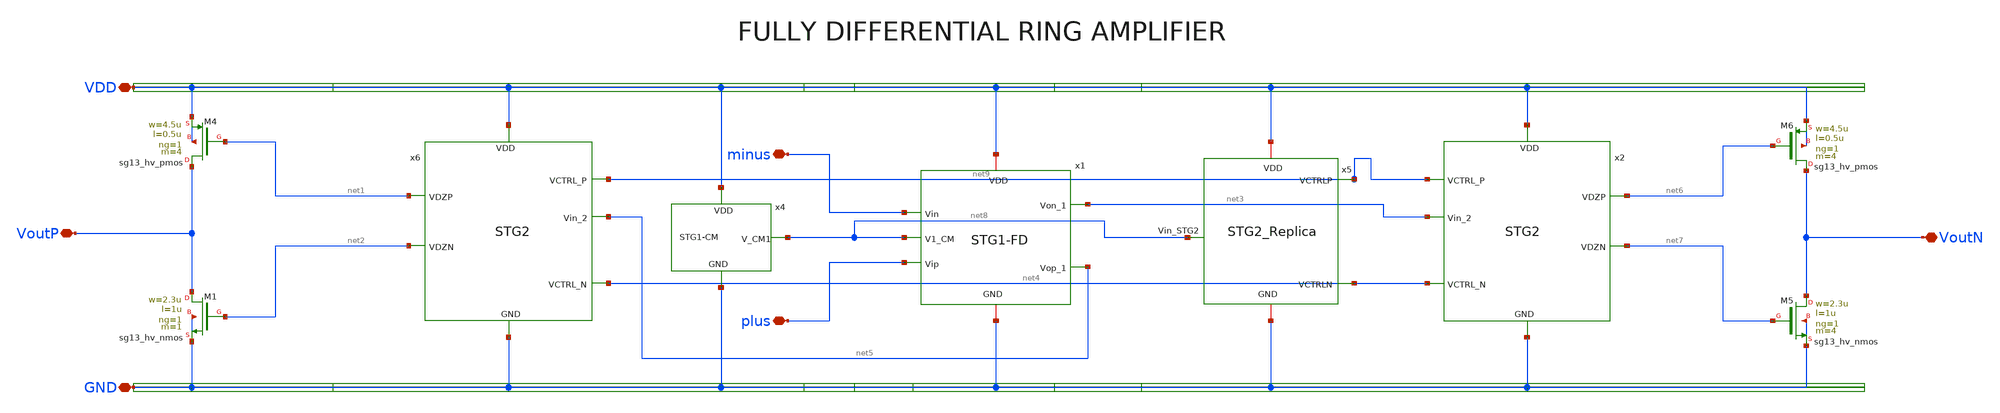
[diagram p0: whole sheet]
** sch_path: Design Files/RAMP/Fully-Diff-RAMP/RAMP-FD.sch
**.subckt RAMP-FD GND VDD plus minus VoutP VoutN
*.iopin GND
*.iopin VDD
*.iopin plus
*.iopin minus
*.iopin VoutP
*.iopin VoutN
x2 VDD net9 net6 net3 net7 net4 GND STG2
XM1 VoutP net2 GND GND sg13_hv_nmos w=2.3u l=1u ng=1 m=1 mm_ok=1
XM4 VoutP net1 VDD VDD sg13_hv_pmos w=4.5u l=0.5u ng=1 m=4 mm_ok=1
x1 VDD net3 net5 net8 minus plus GND STG1-FD
x4 VDD net8 GND STG1-CM
x5 VDD net9 net8 net4 GND STG2_Replica
x6 VDD net9 net1 net5 net2 net4 GND STG2
XM5 VoutN net7 GND GND sg13_hv_nmos w=2.3u l=1u ng=1 m=4 mm_ok=1
XM6 VoutN net6 VDD VDD sg13_hv_pmos w=4.5u l=0.5u ng=1 m=4 mm_ok=1
**.ends

* expanding   symbol:  /foss/designs/RAMP/Fully-Diff-RAMP/STG2.sym # of pins=7
** sym_path: Design Files/RAMP/Fully-Diff-RAMP/STG2.sym
** sch_path: Design Files/RAMP/Fully-Diff-RAMP/STG2.sch
.subckt STG2 VDD VCTRL_P VDZP Vin_2 VDZN VCTRL_N GND
*.ipin Vin_2
*.ipin VDD
*.ipin GND
*.ipin VCTRL_P
*.ipin VCTRL_N
*.opin VDZN
*.opin VDZP
XMN_STG2_3N1 VDZN Vin_2 GND GND sg13_lv_nmos w=0.15u l=0.13u ng=1 m=1 mm_ok=1
XMN_STG2_3P1 VDZN Vin_2 net1 VDD sg13_lv_pmos w=0.15u l=0.13u ng=1 m=3 mm_ok=1
XMP_DZ_STG2_3N net1 VCTRL_P VDD VDD sg13_lv_pmos w=0.15u l=0.13u ng=1 m=5 mm_ok=1
XMP_STG2_3P2 VDZP Vin_2 net2 net2 sg13_lv_nmos w=0.15u l=0.13u ng=1 m=1 mm_ok=1
XMP_STG2_3P1 VDZP Vin_2 VDD VDD sg13_lv_pmos w=0.15u l=0.13u ng=1 m=1 mm_ok=1
XMN_DZ_STG2_3P net2 VCTRL_N GND GND sg13_lv_nmos w=0.15u l=0.13u ng=1 m=1 mm_ok=1
.ends


* expanding   symbol:  /foss/designs/RAMP/Fully-Diff-RAMP/STG1-FD.sym # of pins=7
** sym_path: Design Files/RAMP/Fully-Diff-RAMP/STG1-FD.sym
** sch_path: Design Files/RAMP/Fully-Diff-RAMP/STG1-FD.sch
.subckt STG1-FD VDD Von_1 Vop_1 V1_CM Vin Vip GND
*.opin Von_1
*.iopin VDD
*.iopin GND
*.opin Vop_1
*.ipin Vip
*.ipin Vin
*.ipin V1_CM
R1 net2 Von_1 100k m=1
R3 net2 Vop_1 100k m=1
XMN_STG1_IP_N1 Von_1 Vip net3 GND sg13_lv_nmos w=1.563u l=0.5u ng=1 m=2 mm_ok=1
XMN_STG1_IP_N2 Vop_1 Vin net3 GND sg13_lv_nmos w=1.563u l=0.5u ng=1 m=2 mm_ok=1
I0 net3 GND 10u
XMP_STG1_CL_P1 Von_1 net1 VDD VDD sg13_hv_pmos w=0.5u l=1u ng=1 m=1 mm_ok=1
XMP_STG1_CL_P2 Vop_1 net1 VDD VDD sg13_hv_pmos w=0.5u l=1u ng=1 m=1 mm_ok=1
E1 net1 GND net2 V1_CM 10k
.ends


* expanding   symbol:  /foss/designs/RAMP/Fully-Diff-RAMP/STG1-CM.sym # of pins=3
** sym_path: Design Files/RAMP/Fully-Diff-RAMP/STG1-CM.sym
** sch_path: Design Files/RAMP/Fully-Diff-RAMP/STG1-CM.sch
.subckt STG1-CM VDD V_CM1 GND
*.ipin VDD
*.ipin GND
*.opin V_CM1
XM9 V_CM1 V_CM1 GND GND sg13_lv_nmos w=0.15u l=0.13u ng=1 m=1 mm_ok=1
XM10 V_CM1 V_CM1 net1 VDD sg13_lv_pmos w=0.15u l=0.13u ng=1 m=3 mm_ok=1
XM11 net1 GND VDD VDD sg13_lv_pmos w=0.15u l=0.13u ng=1 m=5 mm_ok=1
XM12 V_CM1 V_CM1 net2 net2 sg13_lv_nmos w=0.15u l=0.13u ng=1 m=1 mm_ok=1
XM13 V_CM1 V_CM1 VDD VDD sg13_lv_pmos w=0.15u l=0.13u ng=1 m=1 mm_ok=1
XM14 net2 VDD GND GND sg13_lv_nmos w=0.15u l=0.13u ng=1 m=1 mm_ok=1
.ends


* expanding   symbol:  /foss/designs/RAMP/Fully-Diff-RAMP/STG2_Replica.sym # of pins=5
** sym_path: Design Files/RAMP/Fully-Diff-RAMP/STG2_Replica.sym
** sch_path: Design Files/RAMP/Fully-Diff-RAMP/STG2_Replica.sch
.subckt STG2_Replica VDD VCTRLP Vin_STG2 VCTRLN GND
*.ipin Vin_STG2
*.iopin VDD
*.iopin GND
*.opin VCTRLP
*.opin VCTRLN
XMN_STG2_3N1 net1 Vin_STG2 GND GND sg13_lv_nmos w=0.15u l=0.13u ng=1 m=1 mm_ok=1
XMN_STG2_3P1 net1 Vin_STG2 net2 VDD sg13_lv_pmos w=0.15u l=0.13u ng=1 m=3 mm_ok=1
XMP_DZ_STG2_3N net2 VCTRLP VDD VDD sg13_lv_pmos w=0.15u l=0.13u ng=1 m=5 mm_ok=1
XMP_STG2_3P2 net4 Vin_STG2 net3 net3 sg13_lv_nmos w=0.15u l=0.13u ng=1 m=1 mm_ok=1
XMP_STG2_3P1 net4 Vin_STG2 VDD VDD sg13_lv_pmos w=0.15u l=0.13u ng=1 m=1 mm_ok=1
XMN_DZ_STG2_3P net3 VCTRLN GND GND sg13_lv_nmos w=0.15u l=0.13u ng=1 m=1 mm_ok=1
XMN_STG2_3N_R net5 net5 GND GND sg13_hv_nmos w=2.3u l=1u ng=1 m=1 mm_ok=1
I0 VDD net5 1u
x1 VDD net1 net5 VCTRLP GND POTA
XMP_STG2_3P_R net6 net6 VDD VDD sg13_hv_pmos w=4.5u l=0.5u ng=1 m=1 mm_ok=1
I1 net6 GND 1u
x2 VDD VCTRLN net4 net6 GND NOTA
.ends


* expanding   symbol:  /foss/designs/RAMP/OTA/POTA.sym # of pins=5
** sym_path: Design Files/RAMP/OTA/POTA.sym
** sch_path: Design Files/RAMP/OTA/POTA.sch
.subckt POTA VDD PLUS MINUS Vout GND
*.ipin VDD
*.ipin GND
*.ipin PLUS
*.ipin MINUS
*.opin Vout
XM2 net2 PLUS net1 VDD sg13_lv_pmos w=1.2u l=0.5u ng=1 m=2 mm_ok=1
XM3 Vout MINUS net1 VDD sg13_lv_pmos w=1.2u l=0.5u ng=1 m=2 mm_ok=1
XM4 Vout net2 GND GND sg13_hv_nmos w=0.5u l=2u ng=1 m=1 mm_ok=1
XM5 net2 net2 GND GND sg13_hv_nmos w=0.5u l=2u ng=1 m=1 mm_ok=1
I1 VDD net1 2u
.ends


* expanding   symbol:  /foss/designs/RAMP/OTA/NOTA.sym # of pins=5
** sym_path: Design Files/RAMP/OTA/NOTA.sym
** sch_path: Design Files/RAMP/OTA/NOTA.sch
.subckt NOTA VDD Vout PLUS MINUS GND
*.ipin VDD
*.ipin GND
*.ipin PLUS
*.ipin MINUS
*.opin Vout
XM1 net2 PLUS net1 GND sg13_hv_nmos w=1.75u l=1u ng=1 m=2 mm_ok=1
XM2 Vout MINUS net1 GND sg13_hv_nmos w=1.75u l=1u ng=1 m=2 mm_ok=1
I0 net1 GND 2u
XM3 Vout net2 VDD VDD sg13_hv_pmos w=0.5u l=0.75u ng=1 m=1 mm_ok=1
XM4 net2 net2 VDD VDD sg13_hv_pmos w=0.5u l=0.75u ng=1 m=1 mm_ok=1
.ends

.GLOBAL GND
.end
